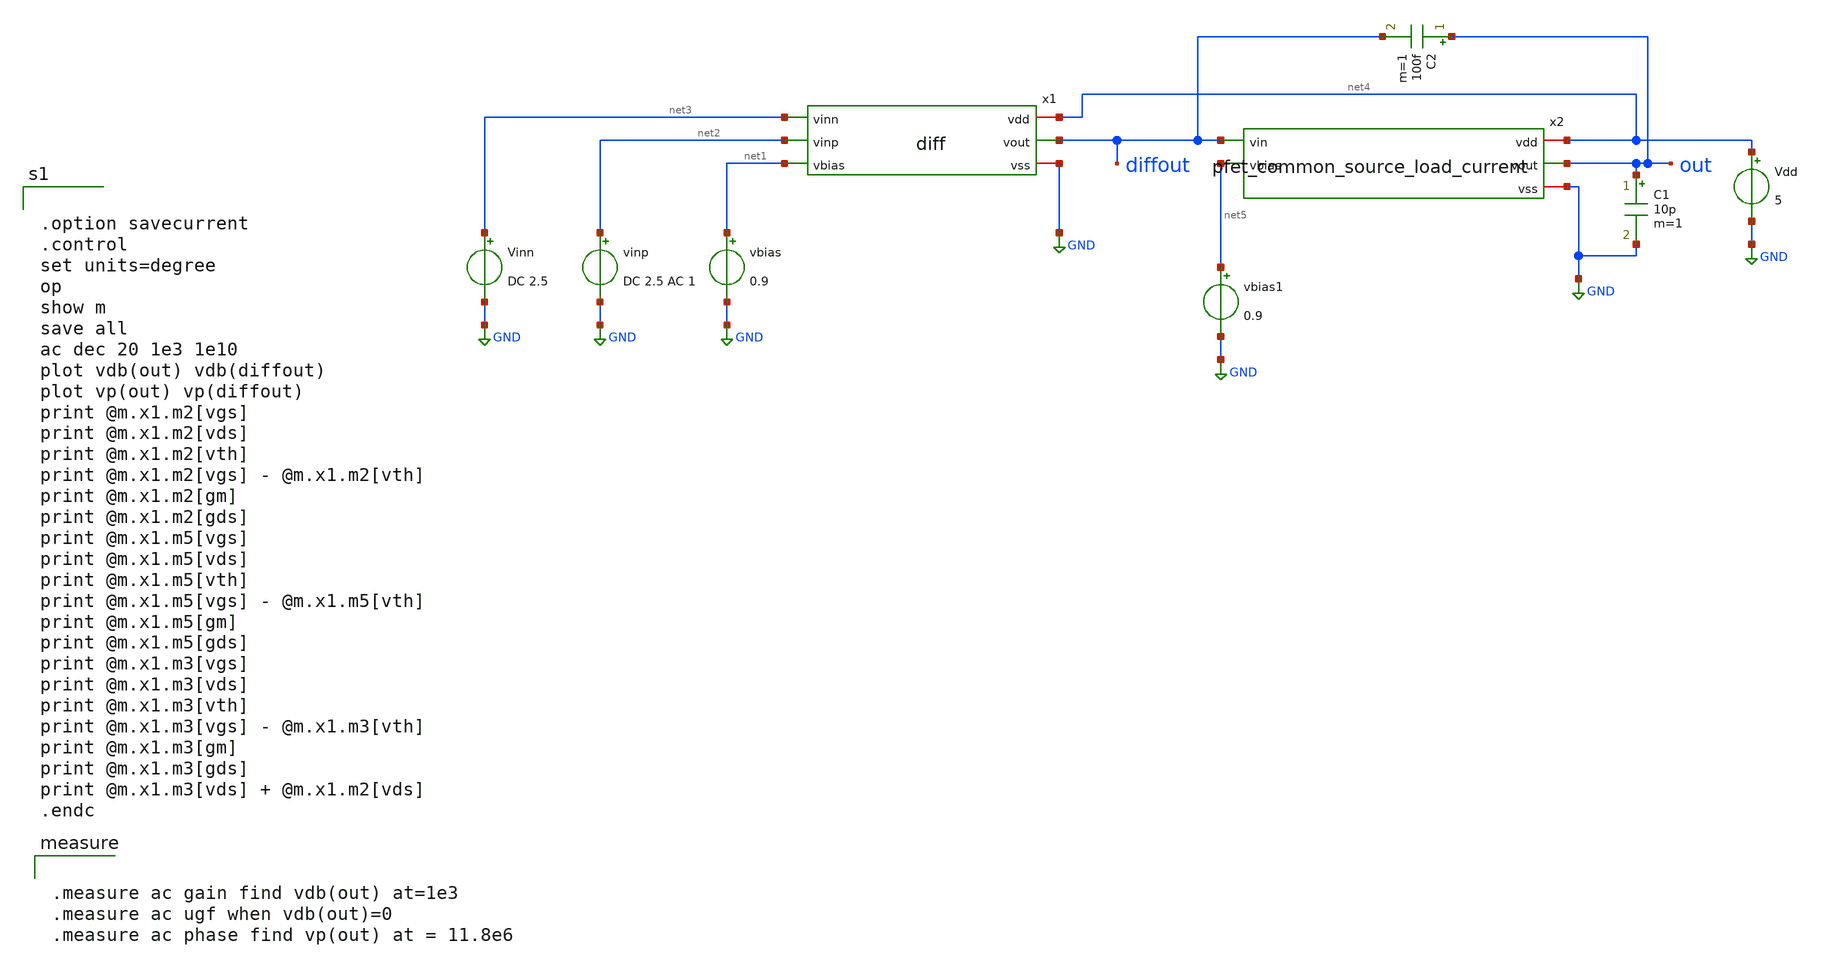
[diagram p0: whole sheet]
** sch_path: member_project/GroupWork/Team_masahiro/diff+source_common+phase_compensation_1.sch
**.subckt diff+source_common+phase_compensation_1
x1 net4 diffout net3 net2 net1 GND diff
x2 net4 diffout out net5 GND pfet_common_source_load_current
Vinn net3 GND DC 2.5
vinp net2 GND DC 2.5 AC 1
vbias net1 GND 0.9
Vdd net4 GND 5
C1 out GND 10p m=1
vbias1 net5 GND 0.9
C2 out diffout 100f m=1
**** begin user architecture code
 .include $::LIB/mos.lib
.include $::LIB/passive.lib
.include $::LIB/diode.lib


.option savecurrent
.control
set units=degree
op
show m
save all
ac dec 20 1e3 1e10
plot vdb(out) vdb(diffout)
plot vp(out) vp(diffout)
print @m.x1.m2[vgs]
print @m.x1.m2[vds]
print @m.x1.m2[vth]
print @m.x1.m2[vgs] - @m.x1.m2[vth]
print @m.x1.m2[gm]
print @m.x1.m2[gds]
print @m.x1.m5[vgs]
print @m.x1.m5[vds]
print @m.x1.m5[vth]
print @m.x1.m5[vgs] - @m.x1.m5[vth]
print @m.x1.m5[gm]
print @m.x1.m5[gds]
print @m.x1.m3[vgs]
print @m.x1.m3[vds]
print @m.x1.m3[vth]
print @m.x1.m3[vgs] - @m.x1.m3[vth]
print @m.x1.m3[gm]
print @m.x1.m3[gds]
print @m.x1.m3[vds] + @m.x1.m2[vds]
.endc




.measure ac gain find vdb(out) at=1e3
.measure ac ugf when vdb(out)=0
.measure ac phase find vp(out) at = 11.8e6


**** end user architecture code
**.ends

* expanding   symbol:  diff.sym # of pins=6
** sym_path: member_project/GroupWork/Team_masahiro/diff.sym
** sch_path: member_project/GroupWork/Team_masahiro/diff.sch
.subckt diff vdd vout vinn vinp vbias vss
*.iopin vss
*.iopin vdd
*.ipin vinn
*.ipin vinp
*.opin vout
*.ipin vbias
M1 net1 vinn net2 vss nmos L=2u W=100u m=1
M2 vout vinp net2 vss nmos L=2u W=100u m=1
M3 net2 vbias vss vss nmos L=2u W=20u m=1
M4 net1 net1 vdd vdd pmos L=2u W=35u m=1
M5 vout net1 vdd vdd pmos L=2u W=35u m=1
.ends


* expanding   symbol:  pfet_common_source_load_current.sym # of pins=5
** sym_path: member_project/GroupWork/Team_masahiro/pfet_common_source_load_current.sym
** sch_path: member_project/GroupWork/Team_masahiro/pfet_common_source_load_current.sch
.subckt pfet_common_source_load_current vdd vin vout vbias vss
*.iopin vss
*.iopin vdd
*.ipin vin
*.opin vout
*.ipin vbias
M1 vout vbias vss vss nmos L=1.0u W=80u m=1
M2 vout vin vdd vdd pmos L=1.0u W=140u m=1
.ends

.GLOBAL GND
.end
